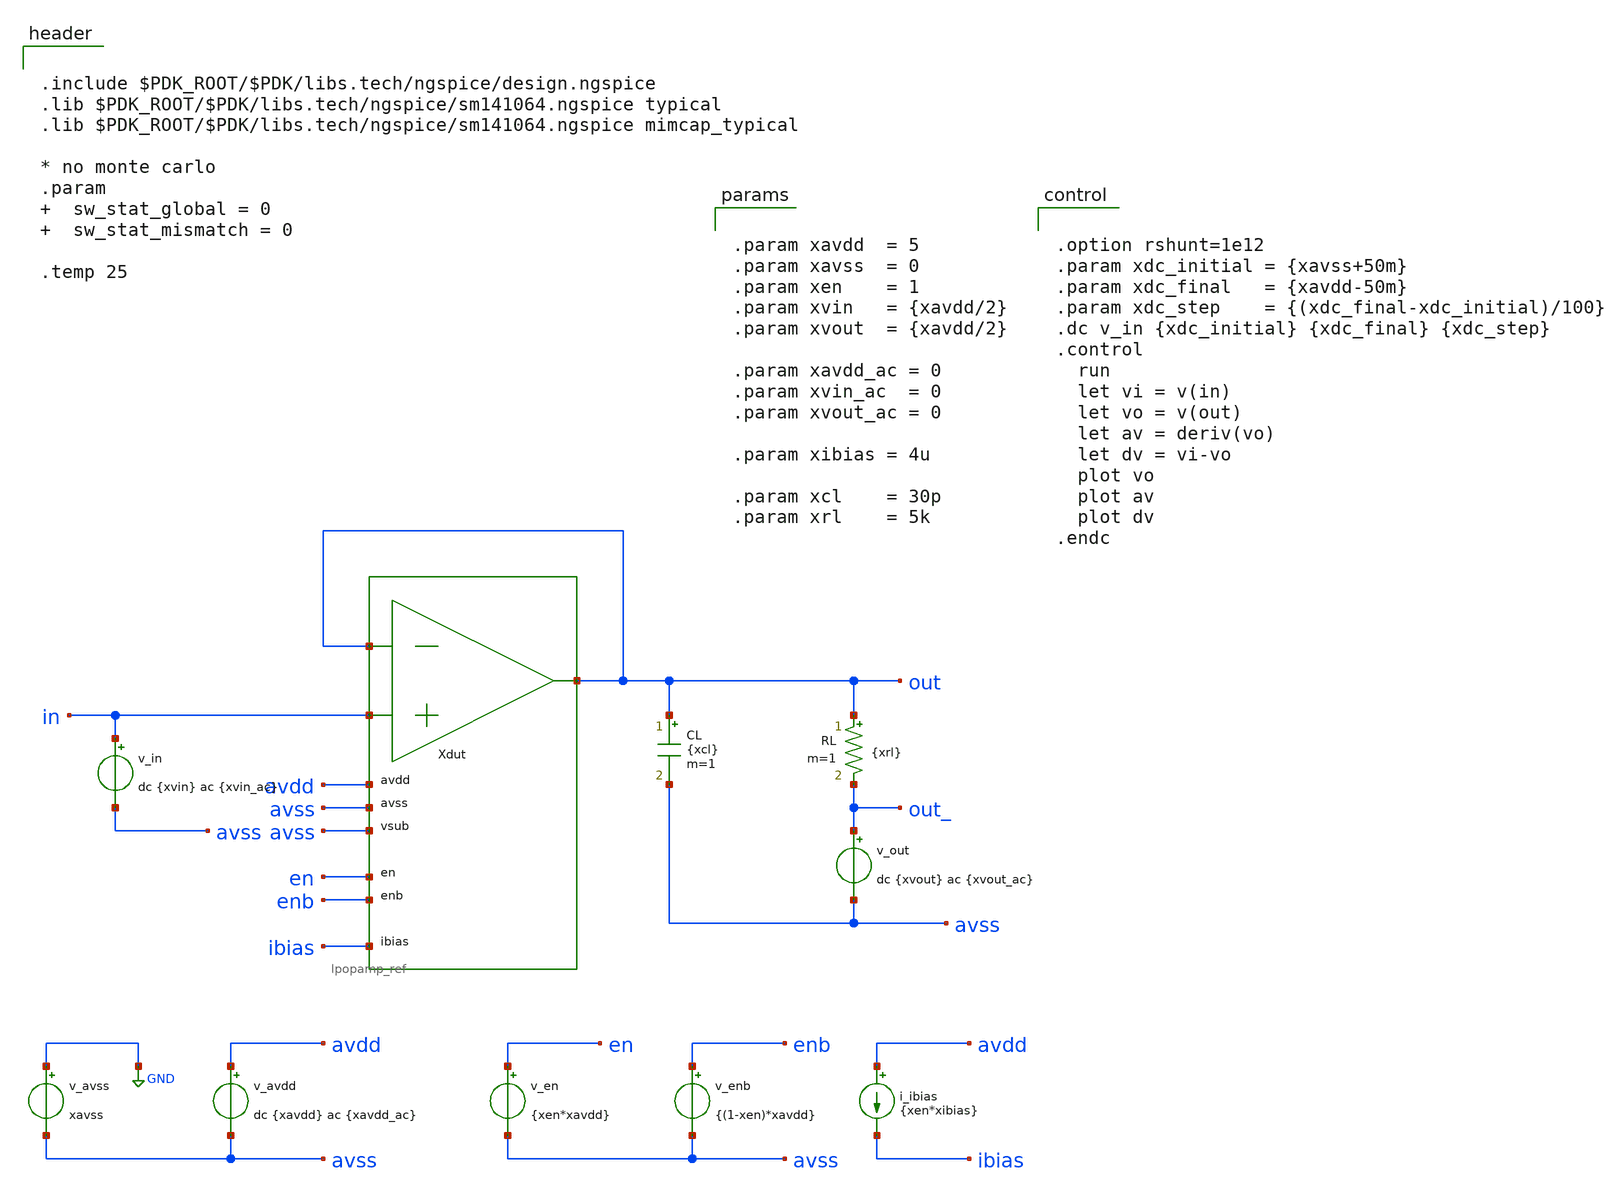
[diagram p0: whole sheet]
** sch_path: xschem/tb_lpopamp_buf_dc.sch
**.subckt tb_lpopamp_buf_dc
Xdut out in out avdd avss avss en enb ibias lpopamp_ref
v_avss GND avss xavss
v_avdd avdd avss dc {xavdd} ac {xavdd_ac}
v_in in avss dc {xvin} ac {xvin_ac}
v_en en avss {xen*xavdd}
v_enb enb avss {(1-xen)*xavdd}
i_ibias avdd ibias {xen*xibias}
CL out avss {xcl} m=1
v_out out_ avss dc {xvout} ac {xvout_ac}
RL out out_ {xrl} m=1
**** begin user architecture code


.include $PDK_ROOT/$PDK/libs.tech/ngspice/design.ngspice
.lib $PDK_ROOT/$PDK/libs.tech/ngspice/sm141064.ngspice typical
.lib $PDK_ROOT/$PDK/libs.tech/ngspice/sm141064.ngspice mimcap_typical

* no monte carlo
.param   sw_stat_global = 0   sw_stat_mismatch = 0

.temp 25




.option rshunt=1e12
.param xdc_initial = {xavss+50m}
.param xdc_final   = {xavdd-50m}
.param xdc_step    = {(xdc_final-xdc_initial)/100}
.dc v_in {xdc_initial} {xdc_final} {xdc_step}
.control
  run
  let vi = v(in)
  let vo = v(out)
  let av = deriv(vo)
  let dv = vi-vo
  plot vo
  plot av
  plot dv
.endc




.param xavdd  = 5
.param xavss  = 0
.param xen    = 1
.param xvin   = {xavdd/2}
.param xvout  = {xavdd/2}

.param xavdd_ac = 0
.param xvin_ac  = 0
.param xvout_ac = 0

.param xibias = 4u

.param xcl    = 30p
.param xrl    = 5k


**** end user architecture code
**.ends
.GLOBAL GND
.end
